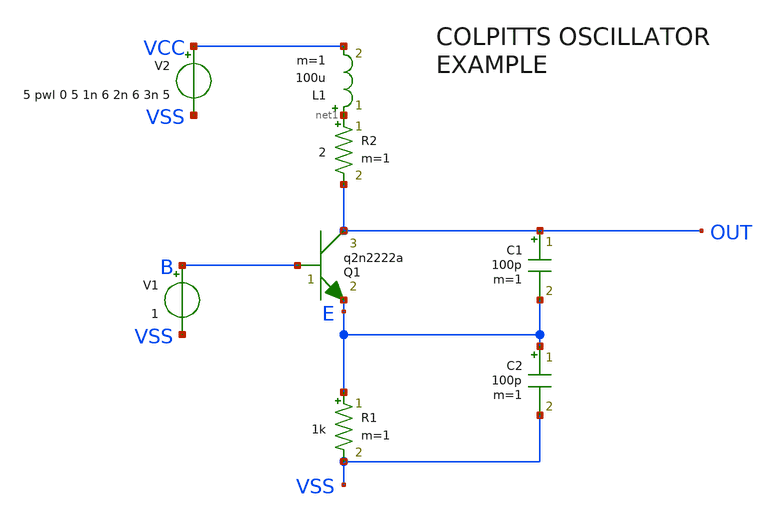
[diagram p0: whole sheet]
** sch_path: xschem_library/examples/osc.sch
**.subckt osc
Q1 OUT B E q2n2222a area=1 m=1
V2 VCC VSS 5 pwl 0 5 1n 6 2n 6 3n 5
L1 net1 VCC 100u m=1
C1 OUT E 100p m=1
V1 B VSS 1
R1 E VSS 1k m=1
R2 net1 OUT 2 m=1
C2 E VSS 100p m=1
**** begin user architecture code

.option RUNLVL=6 post
vvss vss 0 dc 0

.save all
.temp 30
.tran 10n 100u
.probe tran i1(Q1) i2(Q1) i3(Q1) i(L1) i(c1) i(c2) i(r1) i(r2) i(r3)



.MODEL Q2N2222A NPN IS =3.0611E-14 NF =1.00124 BF =220 IKF=0.52                VAF=104 ISE=7.5E-15
+ NE =1.41 NR =1.005 BR =4 IKR=0.24                VAR=28 ISC=1.06525E-11 NC =1.3728 RB =0.13 RE =0.22
+                RC =0.12 CJC=9.12E-12 MJC=0.3508 VJC=0.4089                CJE=27.01E-12 TF =0.325E-9 TR =100E-9
+               vce_max=45 vbe_max=6



**** end user architecture code
**.ends
.end
